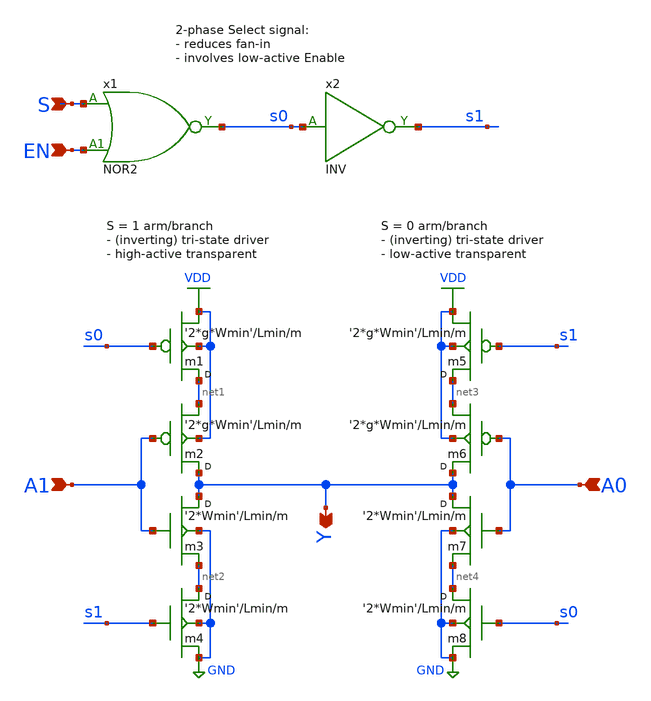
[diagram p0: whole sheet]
** sch_path: Sources/crafted/MUXIEN21.sch
**.subckt MUXIEN21 S A1 Y A0 EN
*.ipin S
*.ipin A1
*.opin Y
*.ipin A0
*.ipin EN
x2 s0 s1 VDD GND INV Wmin=1.5u Lmin=1u g=2 m=1
m3 Y A1 net2 GND nmos4 w='2*Wmin' l=Lmin m=m
m2 Y A1 net1 VDD pmos4 w='2*g*Wmin' l=Lmin m=m
m4 net2 s1 GND GND nmos4 w='2*Wmin' l=Lmin m=m
m1 net1 s0 VDD VDD pmos4 w='2*g*Wmin' l=Lmin m=m
m7 Y A0 net4 GND nmos4 w='2*Wmin' l=Lmin m=m
m6 Y A0 net3 VDD pmos4 w='2*g*Wmin' l=Lmin m=m
m8 net4 s0 GND GND nmos4 w='2*Wmin' l=Lmin m=m
m5 net3 s1 VDD VDD pmos4 w='2*g*Wmin' l=Lmin m=m
x1 S EN s0 VDD GND NOR2 Wmin=1.5u Lmin=1u g=2 m=1
**.ends
.GLOBAL VDD
.GLOBAL GND
.end
